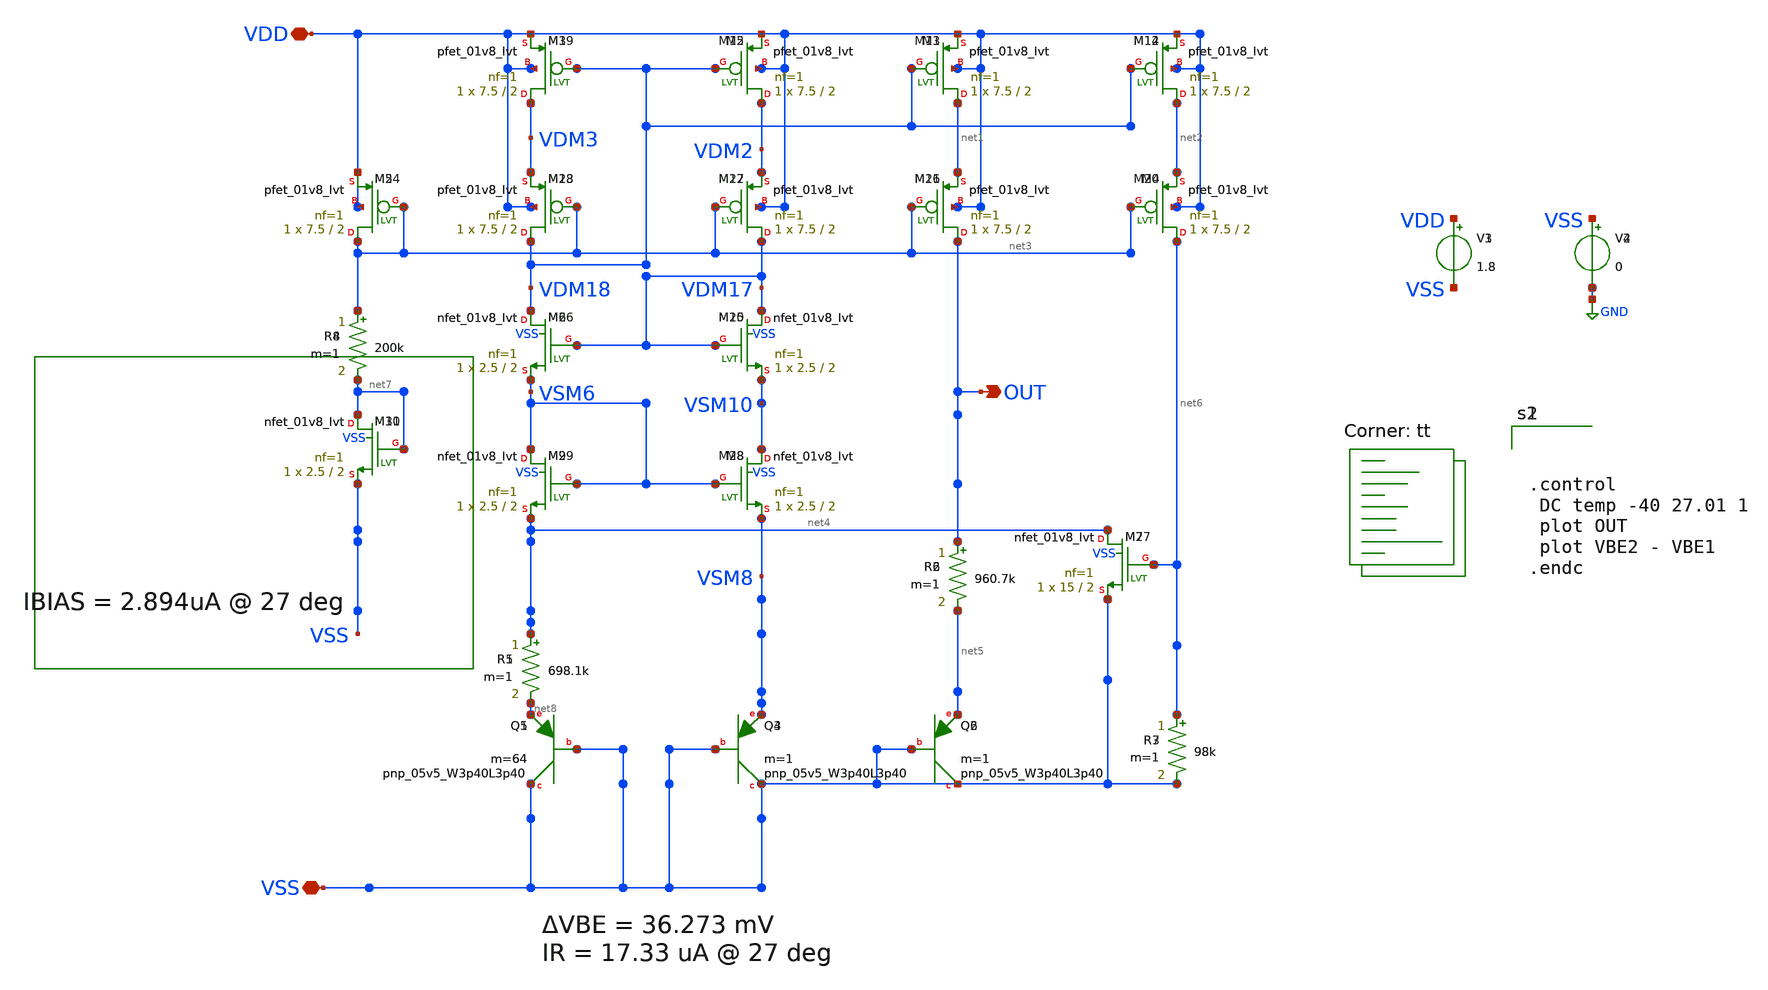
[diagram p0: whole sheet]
** sch_path: bandgap/bgr.sch
**.subckt bgr VDD VSS OUT VDD VSS OUT
*.iopin VDD
*.iopin VSS
*.opin OUT
*.iopin VDD
*.iopin VSS
*.opin OUT
V1 VDD VSS 1.8
V2 VSS GND 0
R1 net4 net8 698.1k m=1
R2 OUT net5 960.7k m=1
R3 net6 VSS 98k m=1
XQ4 VSS VSS VSM8 sky130_fd_pr__pnp_05v5_W3p40L3p40 m=1
XQ1 VSS VSS net8 sky130_fd_pr__pnp_05v5_W3p40L3p40 m=64
XQ2 VSS VSS net5 sky130_fd_pr__pnp_05v5_W3p40L3p40 m=1
XM14 net2 VDM18 VDD VDD sky130_fd_pr__pfet_01v8_lvt L=2 W=7.5 nf=1 ad='int((nf+1)/2) * W/nf * 0.29' as='int((nf+2)/2) * W/nf * 0.29'
+ pd='2*int((nf+1)/2) * (W/nf + 0.29)' ps='2*int((nf+2)/2) * (W/nf + 0.29)' nrd='0.29 / W' nrs='0.29 / W'
+ sa=0 sb=0 sd=0 mult=1 m=1
XM1 net1 VDM18 VDD VDD sky130_fd_pr__pfet_01v8_lvt L=2 W=7.5 nf=1 ad='int((nf+1)/2) * W/nf * 0.29' as='int((nf+2)/2) * W/nf * 0.29'
+ pd='2*int((nf+1)/2) * (W/nf + 0.29)' ps='2*int((nf+2)/2) * (W/nf + 0.29)' nrd='0.29 / W' nrs='0.29 / W'
+ sa=0 sb=0 sd=0 mult=1 m=1
XM2 VDM2 VDM18 VDD VDD sky130_fd_pr__pfet_01v8_lvt L=2 W=7.5 nf=1 ad='int((nf+1)/2) * W/nf * 0.29' as='int((nf+2)/2) * W/nf * 0.29'
+ pd='2*int((nf+1)/2) * (W/nf + 0.29)' ps='2*int((nf+2)/2) * (W/nf + 0.29)' nrd='0.29 / W' nrs='0.29 / W'
+ sa=0 sb=0 sd=0 mult=1 m=1
XM3 VDM3 VDM18 VDD VDD sky130_fd_pr__pfet_01v8_lvt L=2 W=7.5 nf=1 ad='int((nf+1)/2) * W/nf * 0.29' as='int((nf+2)/2) * W/nf * 0.29'
+ pd='2*int((nf+1)/2) * (W/nf + 0.29)' ps='2*int((nf+2)/2) * (W/nf + 0.29)' nrd='0.29 / W' nrs='0.29 / W'
+ sa=0 sb=0 sd=0 mult=1 m=1
XM4 net6 net3 net2 VDD sky130_fd_pr__pfet_01v8_lvt L=2 W=7.5 nf=1 ad='int((nf+1)/2) * W/nf * 0.29' as='int((nf+2)/2) * W/nf * 0.29'
+ pd='2*int((nf+1)/2) * (W/nf + 0.29)' ps='2*int((nf+2)/2) * (W/nf + 0.29)' nrd='0.29 / W' nrs='0.29 / W'
+ sa=0 sb=0 sd=0 mult=1 m=1
XM16 OUT net3 net1 VDD sky130_fd_pr__pfet_01v8_lvt L=2 W=7.5 nf=1 ad='int((nf+1)/2) * W/nf * 0.29' as='int((nf+2)/2) * W/nf * 0.29'
+ pd='2*int((nf+1)/2) * (W/nf + 0.29)' ps='2*int((nf+2)/2) * (W/nf + 0.29)' nrd='0.29 / W' nrs='0.29 / W'
+ sa=0 sb=0 sd=0 mult=1 m=1
XM17 VDM17 net3 VDM2 VDD sky130_fd_pr__pfet_01v8_lvt L=2 W=7.5 nf=1 ad='int((nf+1)/2) * W/nf * 0.29'
+ as='int((nf+2)/2) * W/nf * 0.29' pd='2*int((nf+1)/2) * (W/nf + 0.29)' ps='2*int((nf+2)/2) * (W/nf + 0.29)'
+ nrd='0.29 / W' nrs='0.29 / W' sa=0 sb=0 sd=0 mult=1 m=1
XM18 VDM18 net3 VDM3 VDD sky130_fd_pr__pfet_01v8_lvt L=2 W=7.5 nf=1 ad='int((nf+1)/2) * W/nf * 0.29'
+ as='int((nf+2)/2) * W/nf * 0.29' pd='2*int((nf+1)/2) * (W/nf + 0.29)' ps='2*int((nf+2)/2) * (W/nf + 0.29)'
+ nrd='0.29 / W' nrs='0.29 / W' sa=0 sb=0 sd=0 mult=1 m=1
XM5 net3 net3 VDD VDD sky130_fd_pr__pfet_01v8_lvt L=2 W=7.5 nf=1 ad='int((nf+1)/2) * W/nf * 0.29' as='int((nf+2)/2) * W/nf * 0.29'
+ pd='2*int((nf+1)/2) * (W/nf + 0.29)' ps='2*int((nf+2)/2) * (W/nf + 0.29)' nrd='0.29 / W' nrs='0.29 / W'
+ sa=0 sb=0 sd=0 mult=1 m=1
XM10 VDM17 VDM17 VSM10 VSS sky130_fd_pr__nfet_01v8_lvt L=2 W=2.5 nf=1 ad='int((nf+1)/2) * W/nf * 0.29'
+ as='int((nf+2)/2) * W/nf * 0.29' pd='2*int((nf+1)/2) * (W/nf + 0.29)' ps='2*int((nf+2)/2) * (W/nf + 0.29)'
+ nrd='0.29 / W' nrs='0.29 / W' sa=0 sb=0 sd=0 mult=1 m=1
XM6 VDM18 VDM17 VSM6 VSS sky130_fd_pr__nfet_01v8_lvt L=2 W=2.5 nf=1 ad='int((nf+1)/2) * W/nf * 0.29'
+ as='int((nf+2)/2) * W/nf * 0.29' pd='2*int((nf+1)/2) * (W/nf + 0.29)' ps='2*int((nf+2)/2) * (W/nf + 0.29)'
+ nrd='0.29 / W' nrs='0.29 / W' sa=0 sb=0 sd=0 mult=1 m=1
XM7 net4 net6 VSS VSS sky130_fd_pr__nfet_01v8_lvt L=2 W=15 nf=1 ad='int((nf+1)/2) * W/nf * 0.29' as='int((nf+2)/2) * W/nf * 0.29'
+ pd='2*int((nf+1)/2) * (W/nf + 0.29)' ps='2*int((nf+2)/2) * (W/nf + 0.29)' nrd='0.29 / W' nrs='0.29 / W'
+ sa=0 sb=0 sd=0 mult=1 m=1
XM8 VSM10 VSM6 VSM8 VSS sky130_fd_pr__nfet_01v8_lvt L=2 W=2.5 nf=1 ad='int((nf+1)/2) * W/nf * 0.29' as='int((nf+2)/2) * W/nf * 0.29'
+ pd='2*int((nf+1)/2) * (W/nf + 0.29)' ps='2*int((nf+2)/2) * (W/nf + 0.29)' nrd='0.29 / W' nrs='0.29 / W'
+ sa=0 sb=0 sd=0 mult=1 m=1
XM9 VSM6 VSM6 net4 VSS sky130_fd_pr__nfet_01v8_lvt L=2 W=2.5 nf=1 ad='int((nf+1)/2) * W/nf * 0.29' as='int((nf+2)/2) * W/nf * 0.29'
+ pd='2*int((nf+1)/2) * (W/nf + 0.29)' ps='2*int((nf+2)/2) * (W/nf + 0.29)' nrd='0.29 / W' nrs='0.29 / W'
+ sa=0 sb=0 sd=0 mult=1 m=1
R4 net3 net7 200k m=1
XM11 net7 net7 VSS VSS sky130_fd_pr__nfet_01v8_lvt L=2 W=2.5 nf=1 ad='int((nf+1)/2) * W/nf * 0.29' as='int((nf+2)/2) * W/nf * 0.29'
+ pd='2*int((nf+1)/2) * (W/nf + 0.29)' ps='2*int((nf+2)/2) * (W/nf + 0.29)' nrd='0.29 / W' nrs='0.29 / W'
+ sa=0 sb=0 sd=0 mult=1 m=1
V3 VDD VSS 1.8
V4 VSS GND 0
R5 net4 net8 698.1k m=1
R6 OUT net5 960.7k m=1
R7 net6 VSS 98k m=1
XQ3 VSS VSS VSM8 sky130_fd_pr__pnp_05v5_W3p40L3p40 m=1
XQ5 VSS VSS net8 sky130_fd_pr__pnp_05v5_W3p40L3p40 m=64
XQ6 VSS VSS net5 sky130_fd_pr__pnp_05v5_W3p40L3p40 m=1
XM12 net2 VDM18 VDD VDD sky130_fd_pr__pfet_01v8_lvt L=2 W=7.5 nf=1 ad='int((nf+1)/2) * W/nf * 0.29' as='int((nf+2)/2) * W/nf * 0.29'
+ pd='2*int((nf+1)/2) * (W/nf + 0.29)' ps='2*int((nf+2)/2) * (W/nf + 0.29)' nrd='0.29 / W' nrs='0.29 / W'
+ sa=0 sb=0 sd=0 mult=1 m=1
XM13 net1 VDM18 VDD VDD sky130_fd_pr__pfet_01v8_lvt L=2 W=7.5 nf=1 ad='int((nf+1)/2) * W/nf * 0.29' as='int((nf+2)/2) * W/nf * 0.29'
+ pd='2*int((nf+1)/2) * (W/nf + 0.29)' ps='2*int((nf+2)/2) * (W/nf + 0.29)' nrd='0.29 / W' nrs='0.29 / W'
+ sa=0 sb=0 sd=0 mult=1 m=1
XM15 VDM2 VDM18 VDD VDD sky130_fd_pr__pfet_01v8_lvt L=2 W=7.5 nf=1 ad='int((nf+1)/2) * W/nf * 0.29' as='int((nf+2)/2) * W/nf * 0.29'
+ pd='2*int((nf+1)/2) * (W/nf + 0.29)' ps='2*int((nf+2)/2) * (W/nf + 0.29)' nrd='0.29 / W' nrs='0.29 / W'
+ sa=0 sb=0 sd=0 mult=1 m=1
XM19 VDM3 VDM18 VDD VDD sky130_fd_pr__pfet_01v8_lvt L=2 W=7.5 nf=1 ad='int((nf+1)/2) * W/nf * 0.29' as='int((nf+2)/2) * W/nf * 0.29'
+ pd='2*int((nf+1)/2) * (W/nf + 0.29)' ps='2*int((nf+2)/2) * (W/nf + 0.29)' nrd='0.29 / W' nrs='0.29 / W'
+ sa=0 sb=0 sd=0 mult=1 m=1
XM20 net6 net3 net2 VDD sky130_fd_pr__pfet_01v8_lvt L=2 W=7.5 nf=1 ad='int((nf+1)/2) * W/nf * 0.29' as='int((nf+2)/2) * W/nf * 0.29'
+ pd='2*int((nf+1)/2) * (W/nf + 0.29)' ps='2*int((nf+2)/2) * (W/nf + 0.29)' nrd='0.29 / W' nrs='0.29 / W'
+ sa=0 sb=0 sd=0 mult=1 m=1
XM21 OUT net3 net1 VDD sky130_fd_pr__pfet_01v8_lvt L=2 W=7.5 nf=1 ad='int((nf+1)/2) * W/nf * 0.29' as='int((nf+2)/2) * W/nf * 0.29'
+ pd='2*int((nf+1)/2) * (W/nf + 0.29)' ps='2*int((nf+2)/2) * (W/nf + 0.29)' nrd='0.29 / W' nrs='0.29 / W'
+ sa=0 sb=0 sd=0 mult=1 m=1
XM22 VDM17 net3 VDM2 VDD sky130_fd_pr__pfet_01v8_lvt L=2 W=7.5 nf=1 ad='int((nf+1)/2) * W/nf * 0.29'
+ as='int((nf+2)/2) * W/nf * 0.29' pd='2*int((nf+1)/2) * (W/nf + 0.29)' ps='2*int((nf+2)/2) * (W/nf + 0.29)'
+ nrd='0.29 / W' nrs='0.29 / W' sa=0 sb=0 sd=0 mult=1 m=1
XM23 VDM18 net3 VDM3 VDD sky130_fd_pr__pfet_01v8_lvt L=2 W=7.5 nf=1 ad='int((nf+1)/2) * W/nf * 0.29'
+ as='int((nf+2)/2) * W/nf * 0.29' pd='2*int((nf+1)/2) * (W/nf + 0.29)' ps='2*int((nf+2)/2) * (W/nf + 0.29)'
+ nrd='0.29 / W' nrs='0.29 / W' sa=0 sb=0 sd=0 mult=1 m=1
XM24 net3 net3 VDD VDD sky130_fd_pr__pfet_01v8_lvt L=2 W=7.5 nf=1 ad='int((nf+1)/2) * W/nf * 0.29' as='int((nf+2)/2) * W/nf * 0.29'
+ pd='2*int((nf+1)/2) * (W/nf + 0.29)' ps='2*int((nf+2)/2) * (W/nf + 0.29)' nrd='0.29 / W' nrs='0.29 / W'
+ sa=0 sb=0 sd=0 mult=1 m=1
XM25 VDM17 VDM17 VSM10 VSS sky130_fd_pr__nfet_01v8_lvt L=2 W=2.5 nf=1 ad='int((nf+1)/2) * W/nf * 0.29'
+ as='int((nf+2)/2) * W/nf * 0.29' pd='2*int((nf+1)/2) * (W/nf + 0.29)' ps='2*int((nf+2)/2) * (W/nf + 0.29)'
+ nrd='0.29 / W' nrs='0.29 / W' sa=0 sb=0 sd=0 mult=1 m=1
XM26 VDM18 VDM17 VSM6 VSS sky130_fd_pr__nfet_01v8_lvt L=2 W=2.5 nf=1 ad='int((nf+1)/2) * W/nf * 0.29'
+ as='int((nf+2)/2) * W/nf * 0.29' pd='2*int((nf+1)/2) * (W/nf + 0.29)' ps='2*int((nf+2)/2) * (W/nf + 0.29)'
+ nrd='0.29 / W' nrs='0.29 / W' sa=0 sb=0 sd=0 mult=1 m=1
XM27 net4 net6 VSS VSS sky130_fd_pr__nfet_01v8_lvt L=2 W=15 nf=1 ad='int((nf+1)/2) * W/nf * 0.29' as='int((nf+2)/2) * W/nf * 0.29'
+ pd='2*int((nf+1)/2) * (W/nf + 0.29)' ps='2*int((nf+2)/2) * (W/nf + 0.29)' nrd='0.29 / W' nrs='0.29 / W'
+ sa=0 sb=0 sd=0 mult=1 m=1
XM28 VSM10 VSM6 VSM8 VSS sky130_fd_pr__nfet_01v8_lvt L=2 W=2.5 nf=1 ad='int((nf+1)/2) * W/nf * 0.29'
+ as='int((nf+2)/2) * W/nf * 0.29' pd='2*int((nf+1)/2) * (W/nf + 0.29)' ps='2*int((nf+2)/2) * (W/nf + 0.29)'
+ nrd='0.29 / W' nrs='0.29 / W' sa=0 sb=0 sd=0 mult=1 m=1
XM29 VSM6 VSM6 net4 VSS sky130_fd_pr__nfet_01v8_lvt L=2 W=2.5 nf=1 ad='int((nf+1)/2) * W/nf * 0.29' as='int((nf+2)/2) * W/nf * 0.29'
+ pd='2*int((nf+1)/2) * (W/nf + 0.29)' ps='2*int((nf+2)/2) * (W/nf + 0.29)' nrd='0.29 / W' nrs='0.29 / W'
+ sa=0 sb=0 sd=0 mult=1 m=1
R8 net3 net7 200k m=1
XM30 net7 net7 VSS VSS sky130_fd_pr__nfet_01v8_lvt L=2 W=2.5 nf=1 ad='int((nf+1)/2) * W/nf * 0.29' as='int((nf+2)/2) * W/nf * 0.29'
+ pd='2*int((nf+1)/2) * (W/nf + 0.29)' ps='2*int((nf+2)/2) * (W/nf + 0.29)' nrd='0.29 / W' nrs='0.29 / W'
+ sa=0 sb=0 sd=0 mult=1 m=1
**** begin user architecture code
.lib $::SKYWATER_MODELS/sky130.lib.spice tt



.control
 DC temp -40 27.01 1
 plot OUT
 plot VBE2 - VBE1
.endc


.lib $::SKYWATER_MODELS/sky130.lib.spice tt



.control
 DC temp -40 27.01 1
 plot OUT
 plot VBE2 - VBE1
.endc


**** end user architecture code
**.ends
.GLOBAL GND
.end
